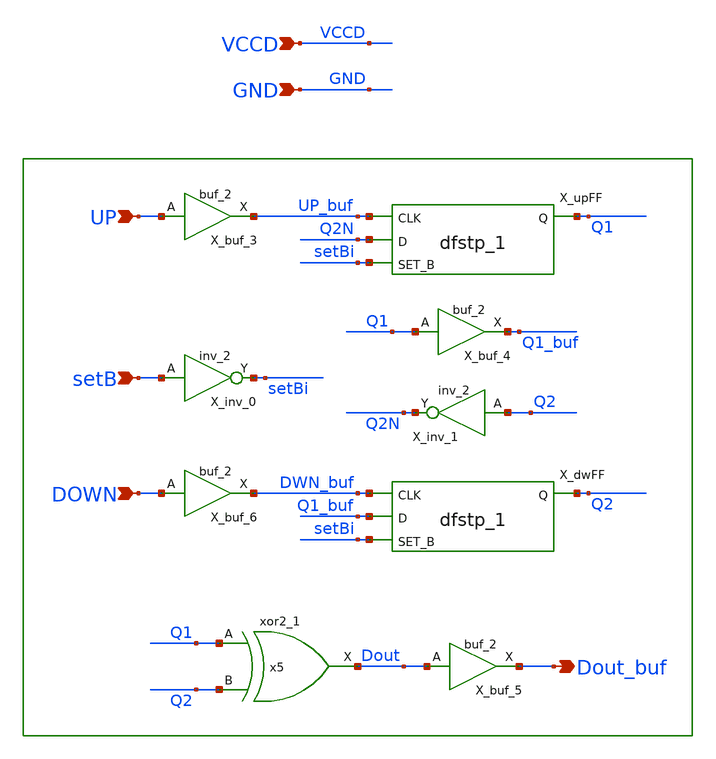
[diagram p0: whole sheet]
** sch_path: xschem/lib_count/count.sch
**.subckt count DOWN Dout_buf GND setB UP VCCD
*.ipin DOWN
*.opin Dout_buf
*.ipin GND
*.ipin setB
*.ipin UP
*.ipin VCCD
X_inv_0 setB GND GND VCCD VCCD setBi sky130_fd_sc_hd__inv_2
X_upFF UP_buf Q2N setBi GND GND VCCD VCCD Q1 sky130_fd_sc_hd__dfstp_1
X_dwFF DWN_buf Q1_buf setBi GND GND VCCD VCCD Q2 sky130_fd_sc_hd__dfstp_1
x5 Q1 Q2 GND GND VCCD VCCD Dout sky130_fd_sc_hd__xor2_1
X_buf_3 UP GND GND VCCD VCCD UP_buf sky130_fd_sc_hd__buf_2
X_buf_4 Q1 GND GND VCCD VCCD Q1_buf sky130_fd_sc_hd__buf_2
X_buf_5 Dout GND GND VCCD VCCD Dout_buf sky130_fd_sc_hd__buf_2
X_buf_6 DOWN GND GND VCCD VCCD DWN_buf sky130_fd_sc_hd__buf_2
X_inv_1 Q2 GND GND VCCD VCCD Q2N sky130_fd_sc_hd__inv_2
**.ends
.end
